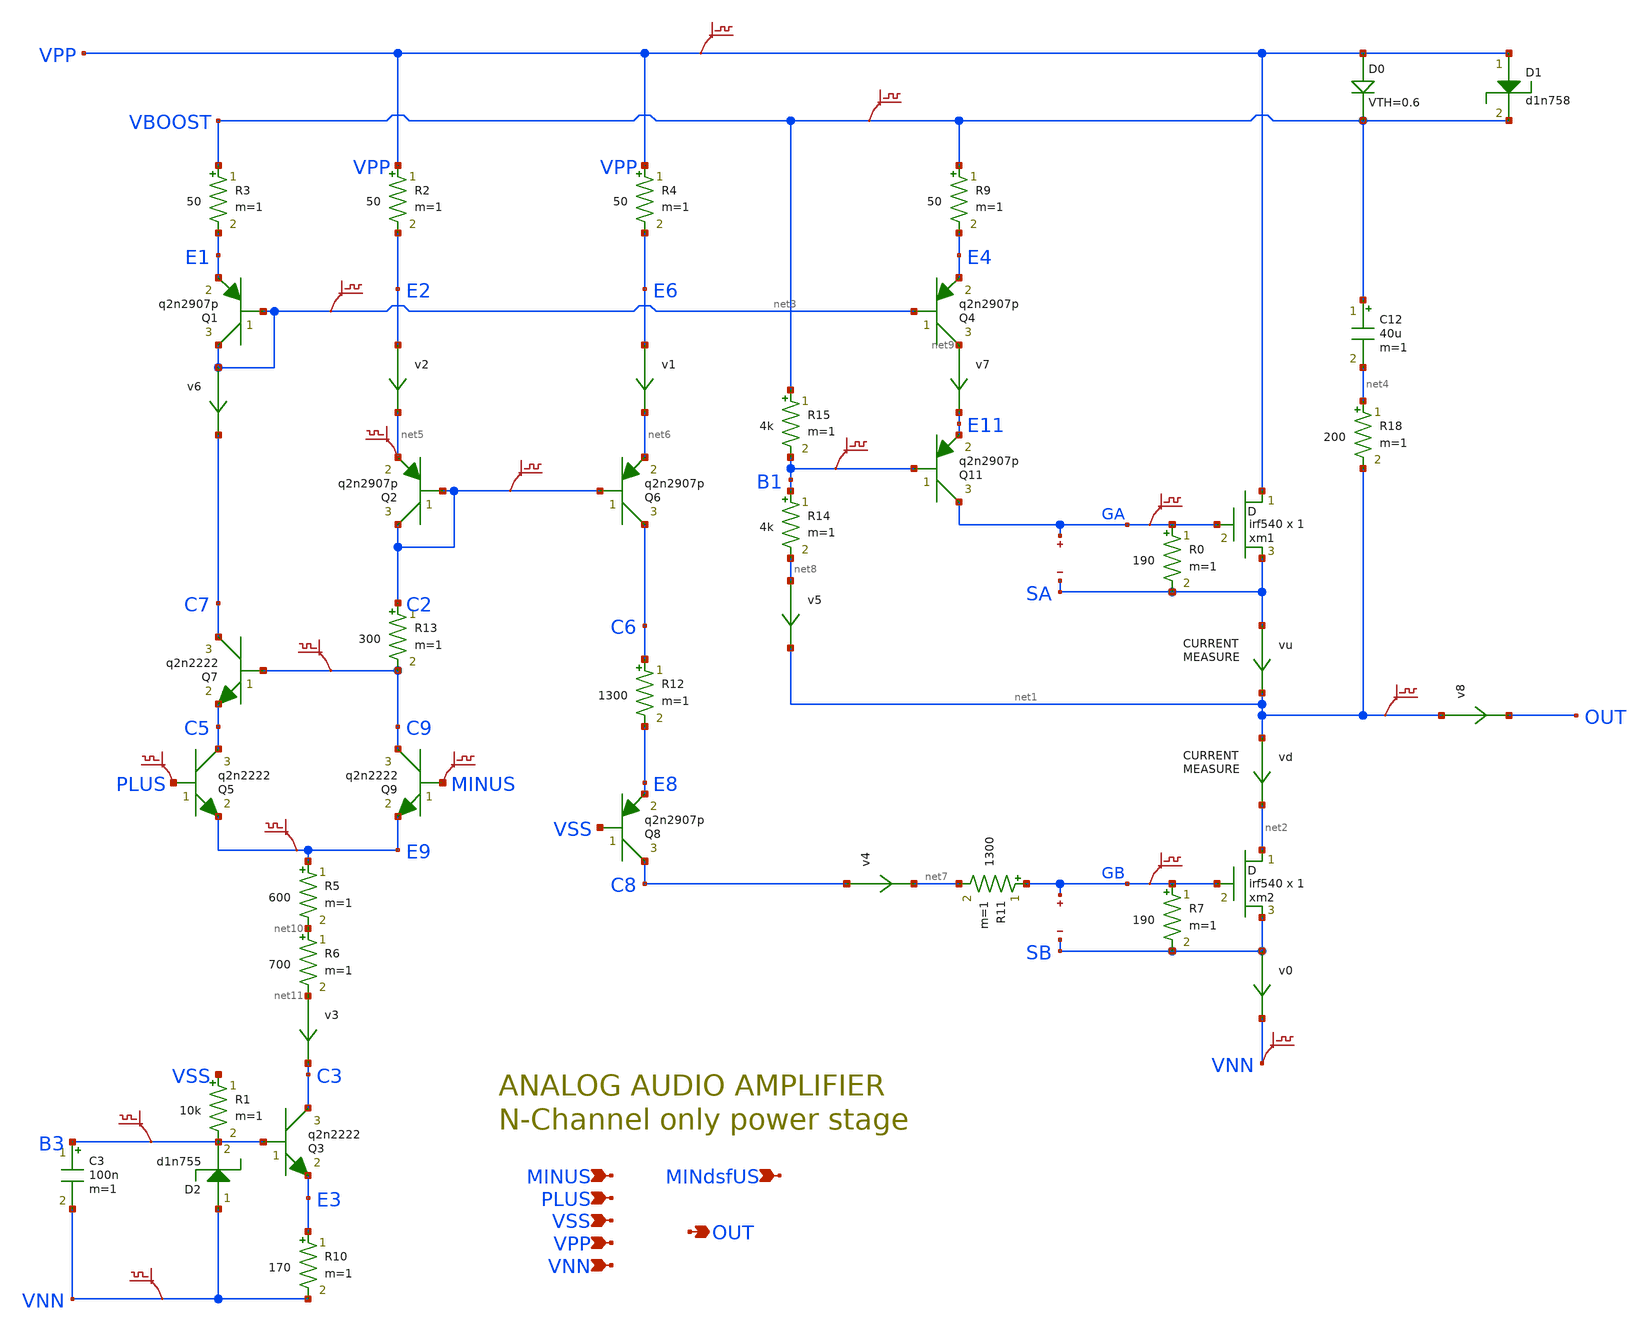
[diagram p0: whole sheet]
** sch_path: xschem_library/examples/mos_power_ampli.sch
**.subckt mos_power_ampli PLUS VPP VNN OUT MINUS VSS MINdsfUS
*.ipin PLUS
*.ipin VPP
*.ipin VNN
*.opin OUT
*.ipin MINUS
*.ipin VSS
*.ipin MINdsfUS
xm2 net2 GB SB irf540 m=1
R7 GB SB 190 m=1
xm1 VPP GA SA irf540 m=1
R0 GA SA 190 m=1
R2 VPP E2 50 m=1
R3 VBOOST E1 50 m=1
Q5 C5 PLUS E9 q2n2222 area=1 m=1
Q4 net9 net3 E4 q2n2907p area=1 m=1
R9 VBOOST E4 50 m=1
Q6 C6 C2 net6 q2n2907p area=1 m=1
R4 VPP E6 50 m=1
vd net1 net2 0
.save i(vd)
vu SA net1 0
.save i(vu)
Q1 net3 net3 E1 q2n2907p area=1 m=1
Q2 C2 C2 net5 q2n2907p area=1 m=1
Q9 C9 MINUS E9 q2n2222 area=1 m=1
R11 GB net7 1300 m=1
Q8 C8 VSS E8 q2n2907p area=1 m=1
C12 VBOOST net4 40u m=1
D0 VPP VBOOST diode VTH=0.6 RON=10 ROFF=1G
R18 net4 net1 200 m=1
D1 VPP VBOOST d1n758
R14 B1 net8 4k m=1
Q11 GA B1 E11 q2n2907p area=1 m=1
R15 VBOOST B1 4k m=1
R5 E9 net10 600 m=1
R6 net10 net11 700 m=1
D2 VNN B3 d1n755
Q3 C3 B3 E3 q2n2222 area=1 m=1
R1 VSS B3 10k m=1
R10 E3 VNN 170 m=1
C3 B3 VNN 100n m=1
R12 C6 E8 1300 m=1
R13 C2 C9 300 m=1
Q7 C7 C9 C5 q2n2222 area=1 m=1
v0 SB VNN 0
.save i(v0)
v1 E6 net6 0
.save i(v1)
v2 E2 net5 0
.save i(v2)
v3 net11 C3 0
.save i(v3)
v4 C8 net7 0
.save i(v4)
v5 net8 net1 0
.save i(v5)
v6 net3 C7 0
.save i(v6)
v7 net9 E11 0
.save i(v7)
.save v(gb)
.save v(gb)
.save v(sb)
.save v(ga)
.save v(sa)
.save v(ga)
.save v(net1)
.save v(minus)
.save v(plus)
.save v(e9)
.save v(c2)
.save v(net3)
.save v(b1)
.save v(vpp)
.save v(vboost)
v8 net1 OUT 0
.save i(v8)
.save v(vnn)
.save v(c9)
.save v(net5)
.save v(b3)
.save v(vnn)
**** begin user architecture code

.option PARHIER=LOCAL RUNLVL=6 post MODMONTE=1 warn maxwarn=6000
.option sampling_method = SRS ingold=1
.option method=gear
.temp 30



vvss vss 0 dc 0
vvpp vpp 0 dc 50
vvnn vnn 0 dc -50

rfb1 vpp minus 100k
rfb2 out minus 100k
rfb3 minus vdc '100k/43'


vvdc vdc 0 dc 21.3
eref vref 0 plus vdc 45

vplus plus vdc dc 0

evboost vboost 0 vol='v(out)>=40 ? v(out)+10 : 50'
rload out 0 4

** models are generally not free: you must download
** SPICE models for active devices and put them  into the below
** referenced file in netlist/simulation directory.
.include "models_poweramp.txt"
.dc vplus '-1.5' '1.5' 0.1
.save all
*.op
*.probe dc v(plus,vdc)



.probe v(ga,sa) v(gb,sb)
.probe p(q*) p(r*) i(r*) p(xm1) p(xm2) i(d*)
**** end user architecture code
**.ends
.end
